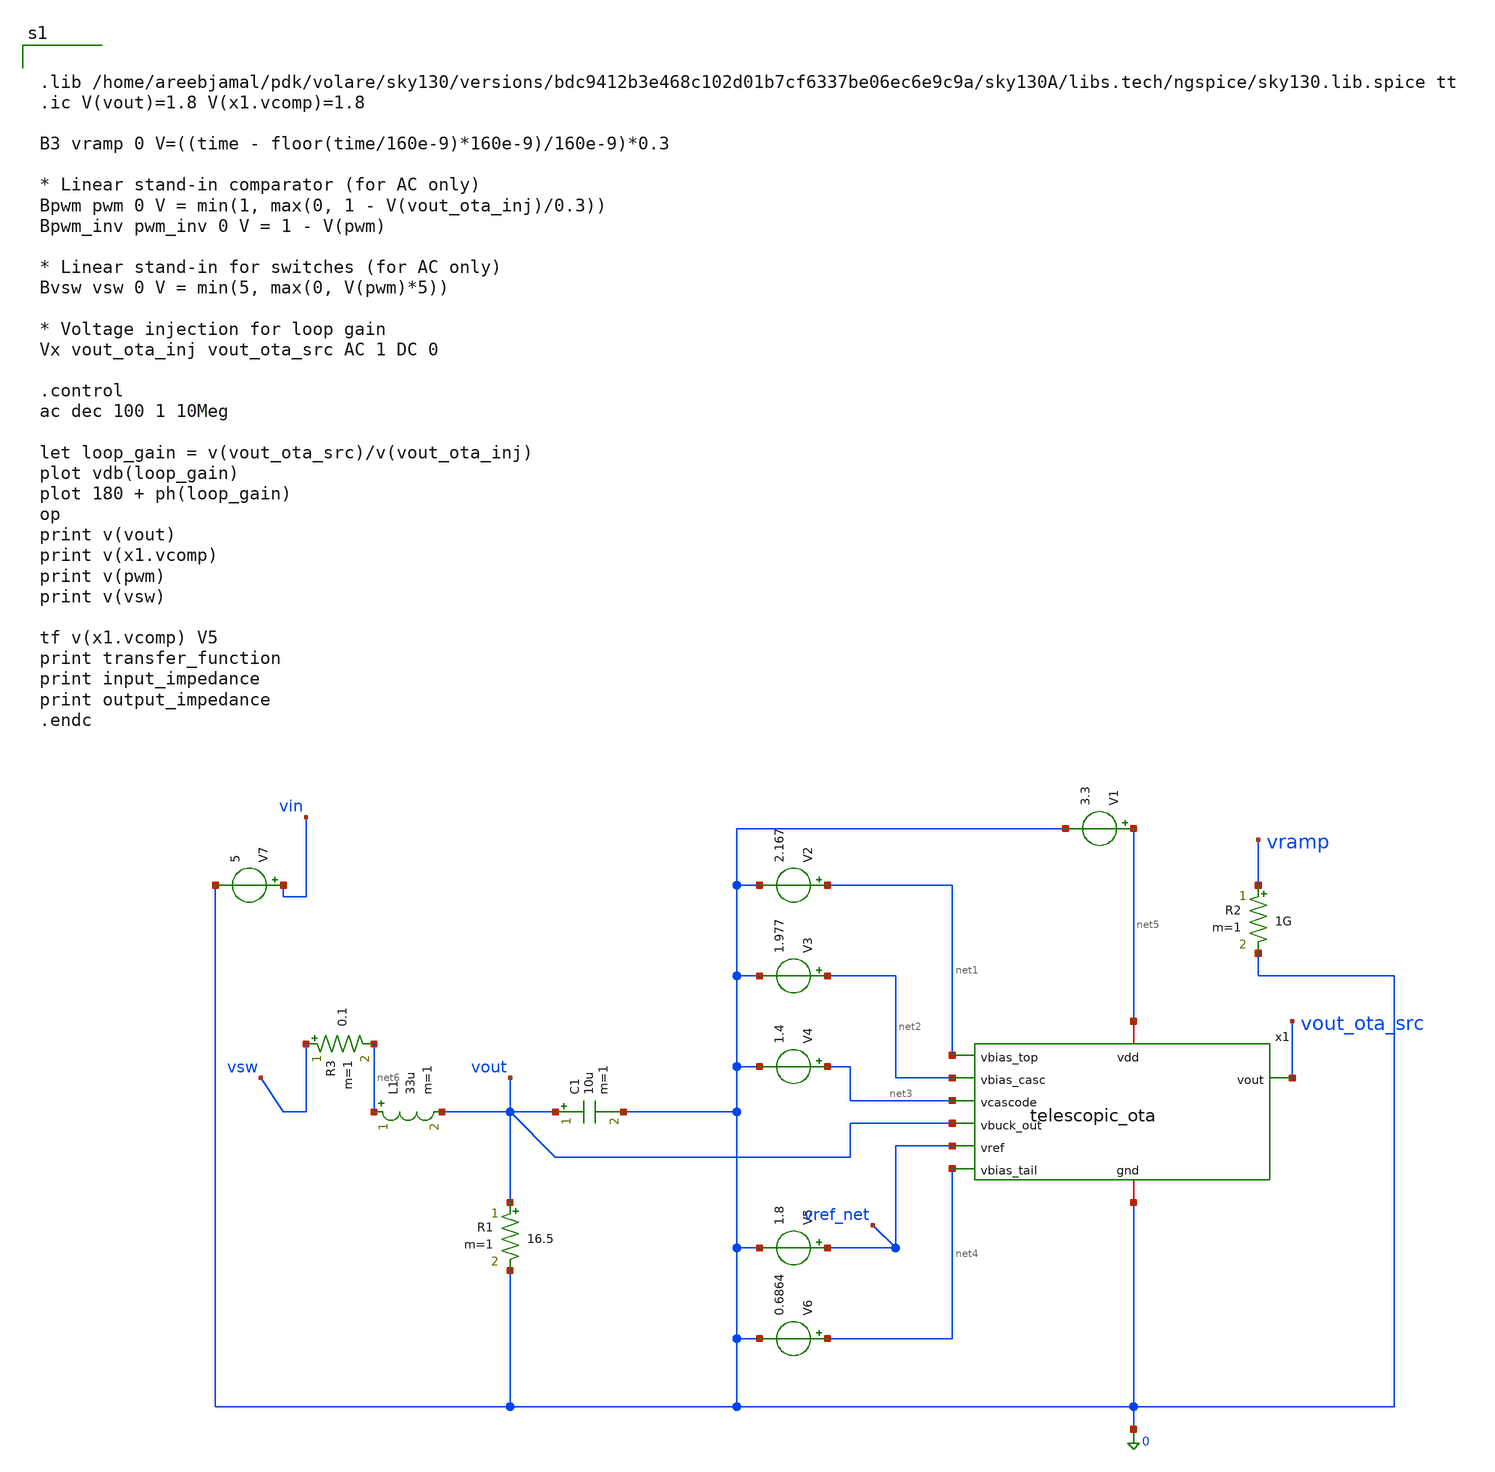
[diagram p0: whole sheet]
** sch_path: CL_Buck_test.sch
**.subckt CL_Buck_test
V1 net5 0 3.3
C1 vout 0 10u m=1
L1 net6 vout 33u m=1
R1 vout 0 16.5 m=1
x1 net5 net1 net2 vout_ota_src net3 vout vref_net net4 0 telescopic_ota
V2 net1 0 2.167
V3 net2 0 1.977
V4 net3 0 1.4
V5 vref_net 0 1.8
V6 net4 0 0.6864
V7 vin 0 5
R2 vramp 0 1G m=1
R3 vsw net6 0.1 m=1
**** begin user architecture code


.lib /home/areebjamal/pdk/volare/sky130/versions/bdc9412b3e468c102d01b7cf6337be06ec6e9c9a/sky130A/libs.tech/ngspice/sky130.lib.spice tt
.ic V(vout)=1.8 V(x1.vcomp)=1.8

B3 vramp 0 V=((time - floor(time/160e-9)*160e-9)/160e-9)*0.3

* Linear stand-in comparator (for AC only)
Bpwm pwm 0 V = min(1, max(0, 1 - V(vout_ota_inj)/0.3))
Bpwm_inv pwm_inv 0 V = 1 - V(pwm)

* Linear stand-in for switches (for AC only)
Bvsw vsw 0 V = min(5, max(0, V(pwm)*5))

* Voltage injection for loop gain
Vx vout_ota_inj vout_ota_src AC 1 DC 0

.control
ac dec 100 1 10Meg

let loop_gain = v(vout_ota_src)/v(vout_ota_inj)
plot vdb(loop_gain)
plot 180 + ph(loop_gain)
op
print v(vout)
print v(x1.vcomp)
print v(pwm)
print v(vsw)

tf v(x1.vcomp) V5
print transfer_function
print input_impedance
print output_impedance
.endc


**** end user architecture code
**.ends

* expanding   symbol:  telescopic_ota.sym # of pins=9
** sym_path: telescopic_ota.sym
** sch_path: telescopic_ota.sch
.subckt telescopic_ota vdd vbias_top vbias_casc vout vcascode vbuck_out vref vbias_tail gnd
*.ipin vbias_top
*.ipin vbias_casc
*.ipin vcascode
*.ipin vbuck_out
*.ipin vref
*.ipin vbias_tail
*.opin vout
*.iopin vdd
*.iopin gnd
XM3 net3 vcascode vy gnd sky130_fd_pr__nfet_01v8 L=1 W=5.6 nf=1 ad='int((1 + 1)/2) * 5.6 / 1 * 0.29'
+ as='int((1 + 2)/2) * 5.6 / 1 * 0.29' pd='2*int((1 + 1)/2) * (5.6 / 1 + 0.29)' ps='2*int((1 + 2)/2) * (5.6 / 1 + 0.29)'
+ nrd='0.29 / 5.6 ' nrs='0.29 / 5.6 ' sa=0 sb=0 sd=0 mult=1 m=1
XM8 net2 vbias_top vdd vdd sky130_fd_pr__pfet_01v8 L=1 W=16.8 nf=1 ad='int((1 + 1)/2) * 16.8 / 1 * 0.29'
+ as='int((1 + 2)/2) * 16.8 / 1 * 0.29' pd='2*int((1 + 1)/2) * (16.8 / 1 + 0.29)' ps='2*int((1 + 2)/2) * (16.8 / 1 + 0.29)'
+ nrd='0.29 / 16.8 ' nrs='0.29 / 16.8 ' sa=0 sb=0 sd=0 mult=1 m=1
XM7 net1 vbias_top vdd vdd sky130_fd_pr__pfet_01v8 L=1 W=16.8 nf=1 ad='int((1 + 1)/2) * 16.8 / 1 * 0.29'
+ as='int((1 + 2)/2) * 16.8 / 1 * 0.29' pd='2*int((1 + 1)/2) * (16.8 / 1 + 0.29)' ps='2*int((1 + 2)/2) * (16.8 / 1 + 0.29)'
+ nrd='0.29 / 16.8 ' nrs='0.29 / 16.8 ' sa=0 sb=0 sd=0 mult=1 m=1
XM5 net3 vbias_casc net1 vdd sky130_fd_pr__pfet_01v8 L=1 W=16.8 nf=1 ad='int((1 + 1)/2) * 16.8 / 1 * 0.29'
+ as='int((1 + 2)/2) * 16.8 / 1 * 0.29' pd='2*int((1 + 1)/2) * (16.8 / 1 + 0.29)' ps='2*int((1 + 2)/2) * (16.8 / 1 + 0.29)'
+ nrd='0.29 / 16.8 ' nrs='0.29 / 16.8 ' sa=0 sb=0 sd=0 mult=1 m=1
XM6 vout vbias_casc net2 vdd sky130_fd_pr__pfet_01v8 L=1 W=16.8 nf=1 ad='int((1 + 1)/2) * 16.8 / 1 * 0.29'
+ as='int((1 + 2)/2) * 16.8 / 1 * 0.29' pd='2*int((1 + 1)/2) * (16.8 / 1 + 0.29)' ps='2*int((1 + 2)/2) * (16.8 / 1 + 0.29)'
+ nrd='0.29 / 16.8 ' nrs='0.29 / 16.8 ' sa=0 sb=0 sd=0 mult=1 m=1
XM1 vy vbuck_out net5 gnd sky130_fd_pr__nfet_01v8 L=1 W=5.6 nf=1 ad='int((1 + 1)/2) * 5.6 / 1 * 0.29'
+ as='int((1 + 2)/2) * 5.6 / 1 * 0.29' pd='2*int((1 + 1)/2) * (5.6 / 1 + 0.29)' ps='2*int((1 + 2)/2) * (5.6 / 1 + 0.29)'
+ nrd='0.29 / 5.6 ' nrs='0.29 / 5.6 ' sa=0 sb=0 sd=0 mult=1 m=1
XM4 vout vcascode net4 gnd sky130_fd_pr__nfet_01v8 L=1 W=5.6 nf=1 ad='int((1 + 1)/2) * 5.6 / 1 * 0.29'
+ as='int((1 + 2)/2) * 5.6 / 1 * 0.29' pd='2*int((1 + 1)/2) * (5.6 / 1 + 0.29)' ps='2*int((1 + 2)/2) * (5.6 / 1 + 0.29)'
+ nrd='0.29 / 5.6 ' nrs='0.29 / 5.6 ' sa=0 sb=0 sd=0 mult=1 m=1
XM2 net4 vref net5 gnd sky130_fd_pr__nfet_01v8 L=1 W=5.6 nf=1 ad='int((1 + 1)/2) * 5.6 / 1 * 0.29' as='int((1 + 2)/2) * 5.6 / 1 * 0.29'
+ pd='2*int((1 + 1)/2) * (5.6 / 1 + 0.29)' ps='2*int((1 + 2)/2) * (5.6 / 1 + 0.29)' nrd='0.29 / 5.6 ' nrs='0.29 / 5.6 '
+ sa=0 sb=0 sd=0 mult=1 m=1
XM9 net5 vbias_tail gnd gnd sky130_fd_pr__nfet_01v8 L=1 W=11.2 nf=1 ad='int((1 + 1)/2) * 11.2 / 1 * 0.29'
+ as='int((1 + 2)/2) * 11.2 / 1 * 0.29' pd='2*int((1 + 1)/2) * (11.2 / 1 + 0.29)' ps='2*int((1 + 2)/2) * (11.2 / 1 + 0.29)'
+ nrd='0.29 / 11.2 ' nrs='0.29 / 11.2 ' sa=0 sb=0 sd=0 mult=1 m=1
R1 vout vcomp 360k m=1
C1 vcomp gnd 100p m=1
.ends

.end
